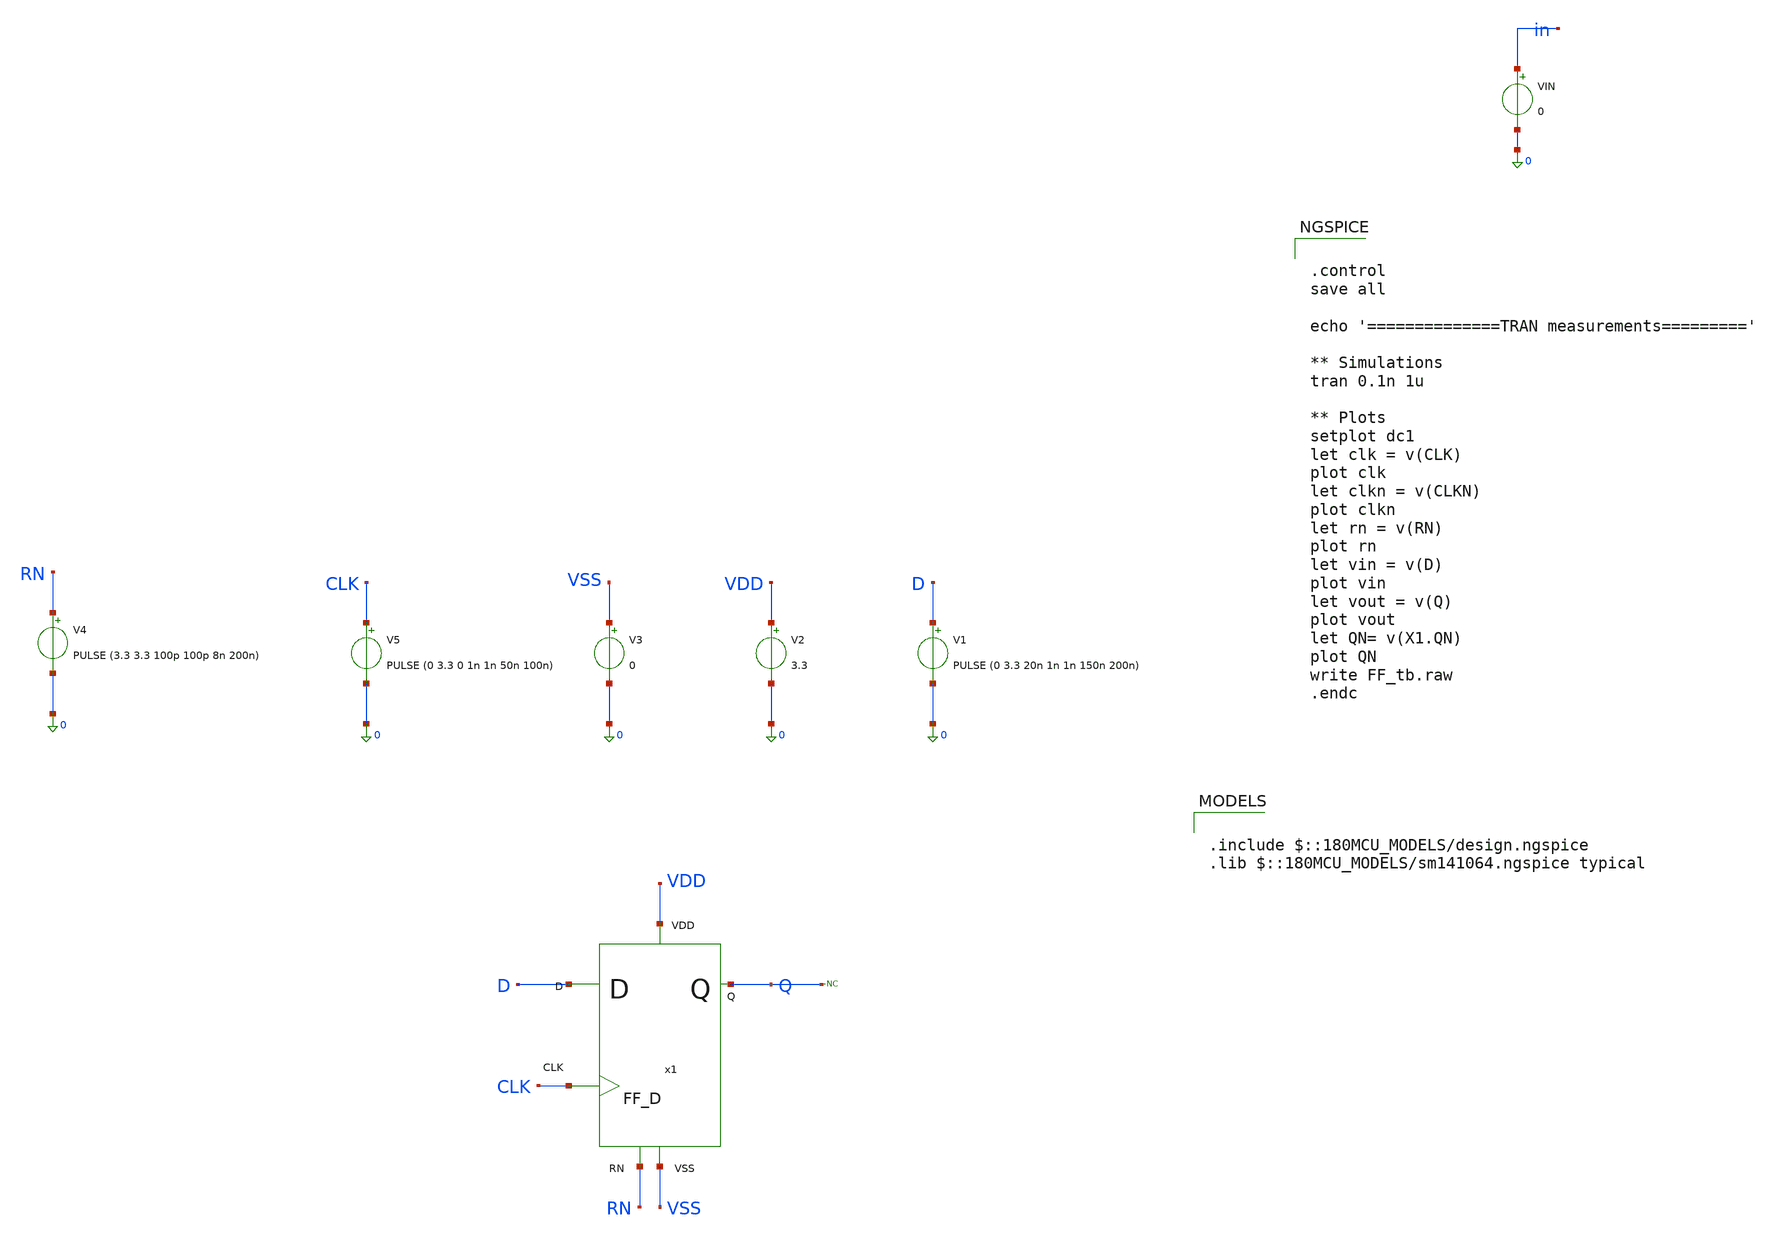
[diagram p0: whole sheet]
** sch_path: designs/sar_adc/digital/flip_flop/xschem/FF_tb.sch
**.subckt FF_tb
V1 D 0 PULSE (0 3.3 20n 1n 1n 150n 200n)
V2 VDD 0 3.3
V3 VSS 0 0
V5 CLK 0 PULSE (0 3.3 0 1n 1n 50n 100n)
x1 CLK D VDD VSS Q RN FF_D
V4 RN 0 PULSE (3.3 3.3 100p 100p 8n 200n)
VIN in 0 0
* noconn Q
**** begin user architecture code

.include $::180MCU_MODELS/design.ngspice
.lib $::180MCU_MODELS/sm141064.ngspice typical



.control
save all

echo '==============TRAN measurements========='

** Simulations
tran 0.1n 1u

** Plots
setplot dc1
let clk = v(CLK)
plot clk
let clkn = v(CLKN)
plot clkn
let rn = v(RN)
plot rn
let vin = v(D)
plot vin
let vout = v(Q)
plot vout
let QN= v(X1.QN)
plot QN
write FF_tb.raw
.endc


**** end user architecture code
**.ends

* expanding   symbol:  sar_adc/digital/flip_flop/xschem/FF_D.sym # of pins=6
** sym_path: designs/sar_adc/digital/flip_flop/xschem/FF_D.sym
** sch_path: designs/sar_adc/digital/flip_flop/xschem/FF_D.sch
.subckt FF_D CLK D VDD VSS Q RN
*.iopin VDD
*.iopin VSS
*.iopin CLK
*.iopin D
*.iopin Q
*.iopin RN
x1 CLK D VDD tg1 CLKN VSS TG
x2 CLK2 net1 VDD net2 CLK2N VSS TG
x3 CLK QN VDD net2 CLKN VSS TG
x4 CLK2 net1 VDD tg1 CLK2N VSS TG
x5 VDD VSS RN tg1 nand1 NAND
x6 VDD VSS RN net3 QN NAND
x8 VDD nand1 net1 VSS inverter
x9 VDD CLK CLK2 VSS inverter
x7 VDD net2 net3 VSS inverter
x10 VDD CLK CLKN VSS inverter
x11 VDD CLK2 CLK2N VSS inverter
x12 VDD QN Q VSS inverter
.ends


* expanding   symbol:  sar_adc/digital/TG/xschem/TG.sym # of pins=6
** sym_path: designs/sar_adc/digital/TG/xschem/TG.sym
** sch_path: designs/sar_adc/digital/TG/xschem/TG.sch
.subckt TG CLK A VDD B CLKN VSS
*.iopin VDD
*.iopin VSS
*.ipin CLK
*.ipin CLKN
*.iopin A
*.iopin B
XM1 A CLK B VSS nfet_03v3 L=0.28u W=0.22u nf=1 ad='int((nf+1)/2) * W/nf * 0.18u' as='int((nf+2)/2) * W/nf * 0.18u'
+ pd='2*int((nf+1)/2) * (W/nf + 0.18u)' ps='2*int((nf+2)/2) * (W/nf + 0.18u)' nrd='0.18u / W' nrs='0.18u / W'
+ sa=0 sb=0 sd=0 m=1
XM2 A CLKN B VDD pfet_03v3 L=0.28u W=0.22u nf=1 ad='int((nf+1)/2) * W/nf * 0.18u' as='int((nf+2)/2) * W/nf * 0.18u'
+ pd='2*int((nf+1)/2) * (W/nf + 0.18u)' ps='2*int((nf+2)/2) * (W/nf + 0.18u)' nrd='0.18u / W' nrs='0.18u / W'
+ sa=0 sb=0 sd=0 m=1
.ends


* expanding   symbol:  sar_adc/digital/NAND/xschem/NAND.sym # of pins=5
** sym_path: designs/sar_adc/digital/NAND/xschem/NAND.sym
** sch_path: designs/sar_adc/digital/NAND/xschem/NAND.sch
.subckt NAND VDD VSS A B out
*.iopin VDD
*.iopin A
*.iopin B
*.iopin out
*.iopin VSS
x1 VDD net1 net2 VSS inverter
x2 VDD net2 out VSS inverter
XM2 net1 A VDD VDD pfet_03v3 L=0.28u W=0.22u nf=1 ad='int((nf+1)/2) * W/nf * 0.18u' as='int((nf+2)/2) * W/nf * 0.18u'
+ pd='2*int((nf+1)/2) * (W/nf + 0.18u)' ps='2*int((nf+2)/2) * (W/nf + 0.18u)' nrd='0.18u / W' nrs='0.18u / W'
+ sa=0 sb=0 sd=0 m=1
XM1 net1 A net3 VSS nfet_03v3 L=0.28u W=0.22u nf=1 ad='int((nf+1)/2) * W/nf * 0.18u' as='int((nf+2)/2) * W/nf * 0.18u'
+ pd='2*int((nf+1)/2) * (W/nf + 0.18u)' ps='2*int((nf+2)/2) * (W/nf + 0.18u)' nrd='0.18u / W' nrs='0.18u / W'
+ sa=0 sb=0 sd=0 m=1
XM3 net1 B VDD VDD pfet_03v3 L=0.28u W=0.22u nf=1 ad='int((nf+1)/2) * W/nf * 0.18u' as='int((nf+2)/2) * W/nf * 0.18u'
+ pd='2*int((nf+1)/2) * (W/nf + 0.18u)' ps='2*int((nf+2)/2) * (W/nf + 0.18u)' nrd='0.18u / W' nrs='0.18u / W'
+ sa=0 sb=0 sd=0 m=1
XM4 net3 B VSS VSS nfet_03v3 L=0.28u W=0.22u nf=1 ad='int((nf+1)/2) * W/nf * 0.18u' as='int((nf+2)/2) * W/nf * 0.18u'
+ pd='2*int((nf+1)/2) * (W/nf + 0.18u)' ps='2*int((nf+2)/2) * (W/nf + 0.18u)' nrd='0.18u / W' nrs='0.18u / W'
+ sa=0 sb=0 sd=0 m=1
.ends


* expanding   symbol:  sar_adc/digital/inverter/xschem/inverter.sym # of pins=6
** sym_path: designs/sar_adc/digital/inverter/xschem/inverter.sym
** sch_path: designs/sar_adc/digital/inverter/xschem/inverter.sch
.subckt inverter VDD in out VSS
*.opin out
*.iopin in
*.iopin VDD
*.iopin VSS
XM1 out in VSS VSS nfet_03v3 L=0.28u W=1u nf=1 ad='int((nf+1)/2) * W/nf * 0.18u' as='int((nf+2)/2) * W/nf * 0.18u'
+ pd='2*int((nf+1)/2) * (W/nf + 0.18u)' ps='2*int((nf+2)/2) * (W/nf + 0.18u)' nrd='0.18u / W' nrs='0.18u / W'
+ sa=0 sb=0 sd=0 m=1
XM2 out in VDD VDD pfet_03v3 L=0.28u W=3u nf=1 ad='int((nf+1)/2) * W/nf * 0.18u' as='int((nf+2)/2) * W/nf * 0.18u'
+ pd='2*int((nf+1)/2) * (W/nf + 0.18u)' ps='2*int((nf+2)/2) * (W/nf + 0.18u)' nrd='0.18u / W' nrs='0.18u / W'
+ sa=0 sb=0 sd=0 m=1
.ends

.end
